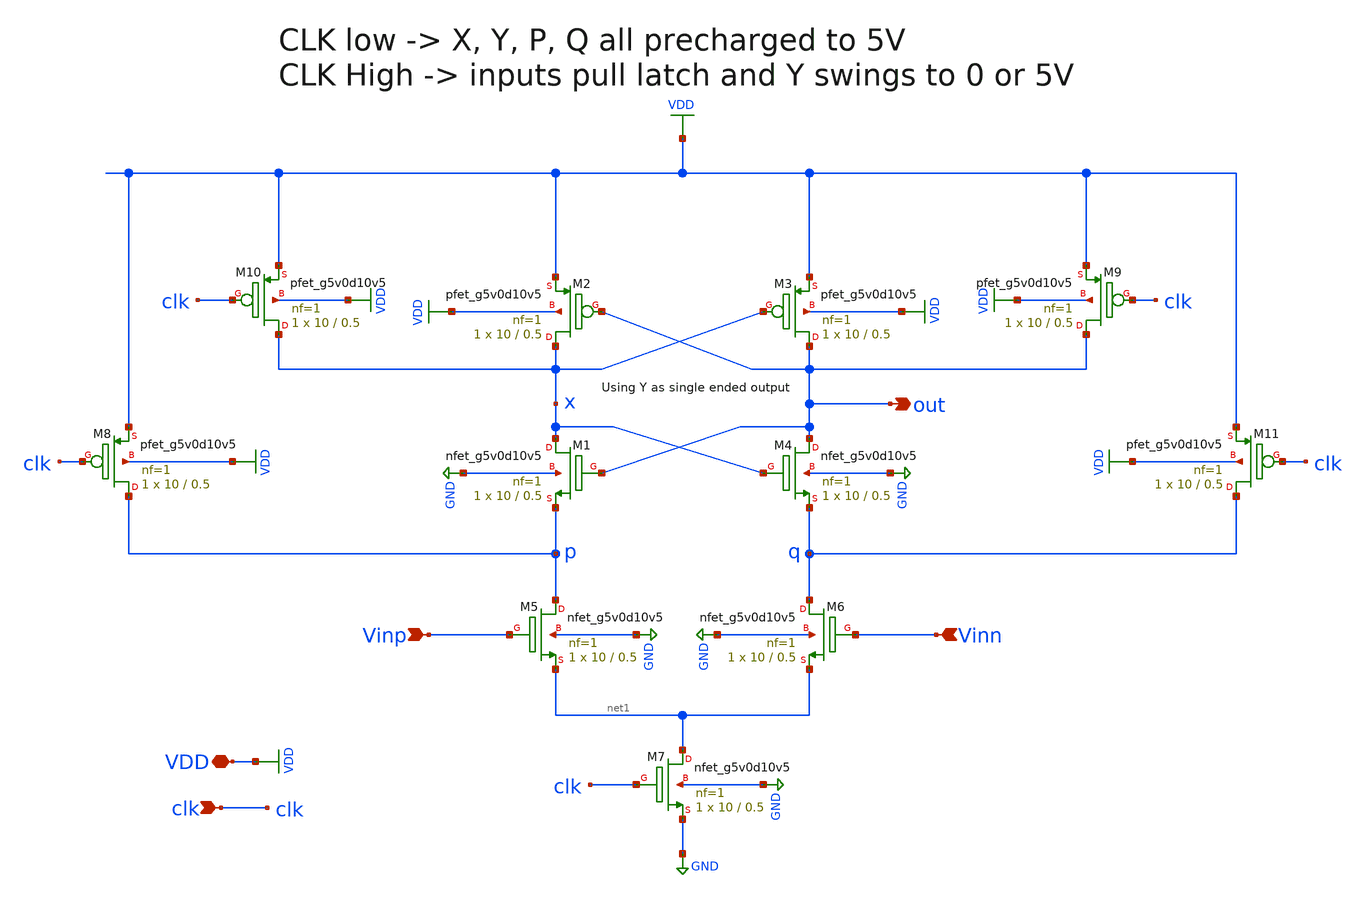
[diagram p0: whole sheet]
** sch_path: ADC/16bit_C2C/MagicAndSpice/strongarm_comp.sch
**.subckt strongarm_comp Vinp Vinn clk VDD out
*.ipin Vinp
*.ipin Vinn
*.ipin clk
*.iopin VDD
*.opin out
XM1 x out p GND sky130_fd_pr__nfet_g5v0d10v5 L=0.5 W=10 nf=1 ad='int((nf+1)/2) * W/nf * 0.29' as='int((nf+2)/2) * W/nf * 0.29'
+ pd='2*int((nf+1)/2) * (W/nf + 0.29)' ps='2*int((nf+2)/2) * (W/nf + 0.29)' nrd='0.29 / W' nrs='0.29 / W'
+ sa=0 sb=0 sd=0 mult=1 m=1
XM2 x out VDD VDD sky130_fd_pr__pfet_g5v0d10v5 L=0.5 W=10 nf=1 ad='int((nf+1)/2) * W/nf * 0.29' as='int((nf+2)/2) * W/nf * 0.29'
+ pd='2*int((nf+1)/2) * (W/nf + 0.29)' ps='2*int((nf+2)/2) * (W/nf + 0.29)' nrd='0.29 / W' nrs='0.29 / W'
+ sa=0 sb=0 sd=0 mult=1 m=1
XM3 out x VDD VDD sky130_fd_pr__pfet_g5v0d10v5 L=0.5 W=10 nf=1 ad='int((nf+1)/2) * W/nf * 0.29' as='int((nf+2)/2) * W/nf * 0.29'
+ pd='2*int((nf+1)/2) * (W/nf + 0.29)' ps='2*int((nf+2)/2) * (W/nf + 0.29)' nrd='0.29 / W' nrs='0.29 / W'
+ sa=0 sb=0 sd=0 mult=1 m=1
XM4 out x q GND sky130_fd_pr__nfet_g5v0d10v5 L=0.5 W=10 nf=1 ad='int((nf+1)/2) * W/nf * 0.29' as='int((nf+2)/2) * W/nf * 0.29'
+ pd='2*int((nf+1)/2) * (W/nf + 0.29)' ps='2*int((nf+2)/2) * (W/nf + 0.29)' nrd='0.29 / W' nrs='0.29 / W'
+ sa=0 sb=0 sd=0 mult=1 m=1
XM5 p Vinp net1 GND sky130_fd_pr__nfet_g5v0d10v5 L=0.5 W=10 nf=1 ad='int((nf+1)/2) * W/nf * 0.29' as='int((nf+2)/2) * W/nf * 0.29'
+ pd='2*int((nf+1)/2) * (W/nf + 0.29)' ps='2*int((nf+2)/2) * (W/nf + 0.29)' nrd='0.29 / W' nrs='0.29 / W'
+ sa=0 sb=0 sd=0 mult=1 m=1
XM6 q Vinn net1 GND sky130_fd_pr__nfet_g5v0d10v5 L=0.5 W=10 nf=1 ad='int((nf+1)/2) * W/nf * 0.29' as='int((nf+2)/2) * W/nf * 0.29'
+ pd='2*int((nf+1)/2) * (W/nf + 0.29)' ps='2*int((nf+2)/2) * (W/nf + 0.29)' nrd='0.29 / W' nrs='0.29 / W'
+ sa=0 sb=0 sd=0 mult=1 m=1
XM7 net1 clk GND GND sky130_fd_pr__nfet_g5v0d10v5 L=0.5 W=10 nf=1 ad='int((nf+1)/2) * W/nf * 0.29' as='int((nf+2)/2) * W/nf * 0.29'
+ pd='2*int((nf+1)/2) * (W/nf + 0.29)' ps='2*int((nf+2)/2) * (W/nf + 0.29)' nrd='0.29 / W' nrs='0.29 / W'
+ sa=0 sb=0 sd=0 mult=1 m=1
XM9 out clk VDD VDD sky130_fd_pr__pfet_g5v0d10v5 L=0.5 W=10 nf=1 ad='int((nf+1)/2) * W/nf * 0.29' as='int((nf+2)/2) * W/nf * 0.29'
+ pd='2*int((nf+1)/2) * (W/nf + 0.29)' ps='2*int((nf+2)/2) * (W/nf + 0.29)' nrd='0.29 / W' nrs='0.29 / W'
+ sa=0 sb=0 sd=0 mult=1 m=1
XM10 x clk VDD VDD sky130_fd_pr__pfet_g5v0d10v5 L=0.5 W=10 nf=1 ad='int((nf+1)/2) * W/nf * 0.29' as='int((nf+2)/2) * W/nf * 0.29'
+ pd='2*int((nf+1)/2) * (W/nf + 0.29)' ps='2*int((nf+2)/2) * (W/nf + 0.29)' nrd='0.29 / W' nrs='0.29 / W'
+ sa=0 sb=0 sd=0 mult=1 m=1
XM8 p clk VDD VDD sky130_fd_pr__pfet_g5v0d10v5 L=0.5 W=10 nf=1 ad='int((nf+1)/2) * W/nf * 0.29' as='int((nf+2)/2) * W/nf * 0.29'
+ pd='2*int((nf+1)/2) * (W/nf + 0.29)' ps='2*int((nf+2)/2) * (W/nf + 0.29)' nrd='0.29 / W' nrs='0.29 / W'
+ sa=0 sb=0 sd=0 mult=1 m=1
XM11 q clk VDD VDD sky130_fd_pr__pfet_g5v0d10v5 L=0.5 W=10 nf=1 ad='int((nf+1)/2) * W/nf * 0.29' as='int((nf+2)/2) * W/nf * 0.29'
+ pd='2*int((nf+1)/2) * (W/nf + 0.29)' ps='2*int((nf+2)/2) * (W/nf + 0.29)' nrd='0.29 / W' nrs='0.29 / W'
+ sa=0 sb=0 sd=0 mult=1 m=1
**.ends
.GLOBAL GND
.GLOBAL VDD
.end
